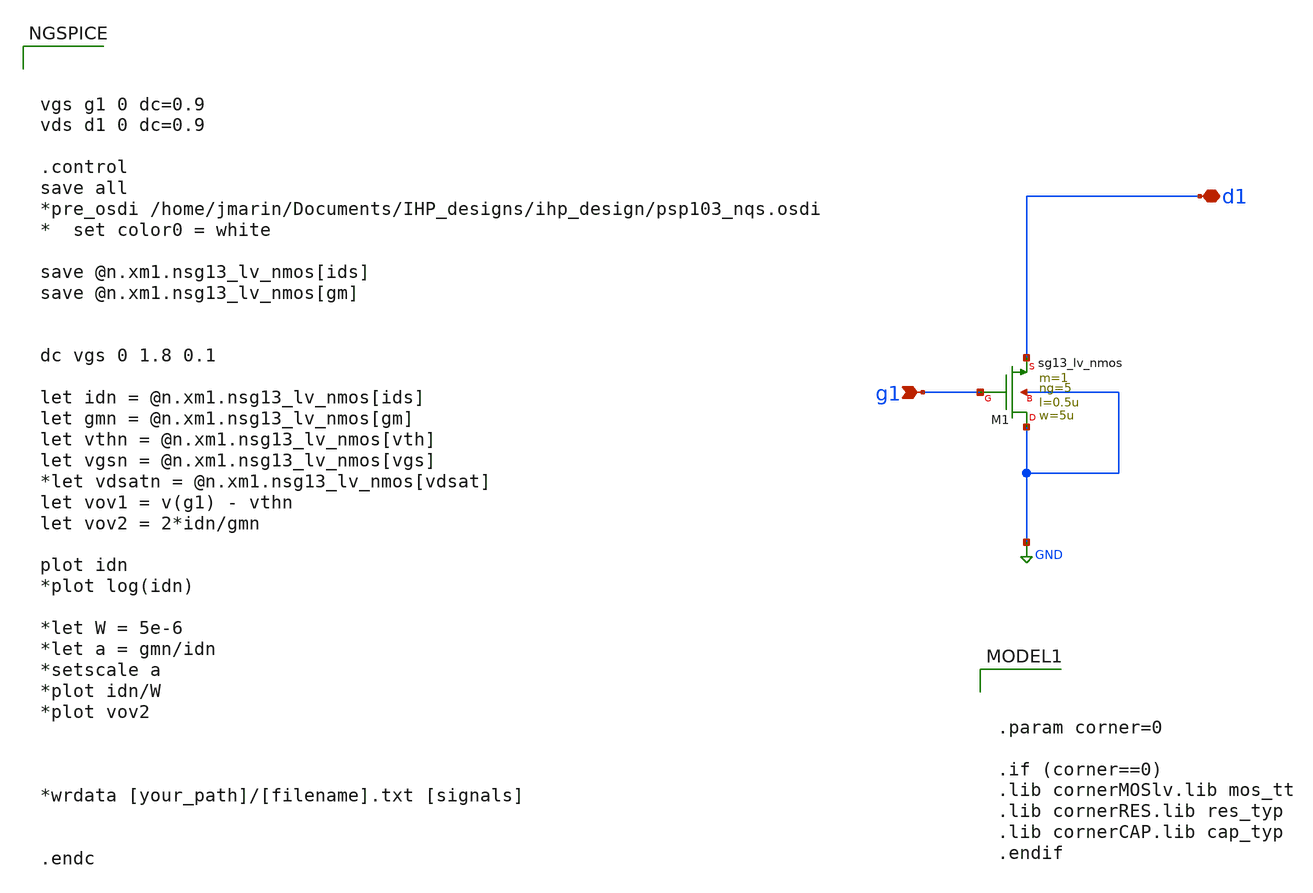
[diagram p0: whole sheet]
** sch_path: task1-nmos-charac/sg13_lv_nmos_charac_IHP.sch
**.subckt sg13_lv_nmos_charac_IHP g1 d1
*.ipin g1
*.iopin d1
XM1 GND g1 d1 GND sg13_lv_nmos w=5u l=0.5u ng=5 m=1 mm_ok=1
**** begin user architecture code



vgs g1 0 dc=0.9
vds d1 0 dc=0.9

.control
save all
*pre_osdi /home/jmarin/Documents/IHP_designs/ihp_design/psp103_nqs.osdi
*  set color0 = white

save @n.xm1.nsg13_lv_nmos[ids]
save @n.xm1.nsg13_lv_nmos[gm]


dc vgs 0 1.8 0.1

let idn = @n.xm1.nsg13_lv_nmos[ids]
let gmn = @n.xm1.nsg13_lv_nmos[gm]
let vthn = @n.xm1.nsg13_lv_nmos[vth]
let vgsn = @n.xm1.nsg13_lv_nmos[vgs]
*let vdsatn = @n.xm1.nsg13_lv_nmos[vdsat]
let vov1 = v(g1) - vthn
let vov2 = 2*idn/gmn

plot idn
*plot log(idn)

*let W = 5e-6
*let a = gmn/idn
*setscale a
*plot idn/W
*plot vov2



*wrdata [your_path]/[filename].txt [signals]


.endc




.param corner=0

.if (corner==0)
.lib cornerMOSlv.lib mos_tt
.lib cornerRES.lib res_typ
.lib cornerCAP.lib cap_typ
.endif

**** end user architecture code
**.ends
.GLOBAL GND
.end
